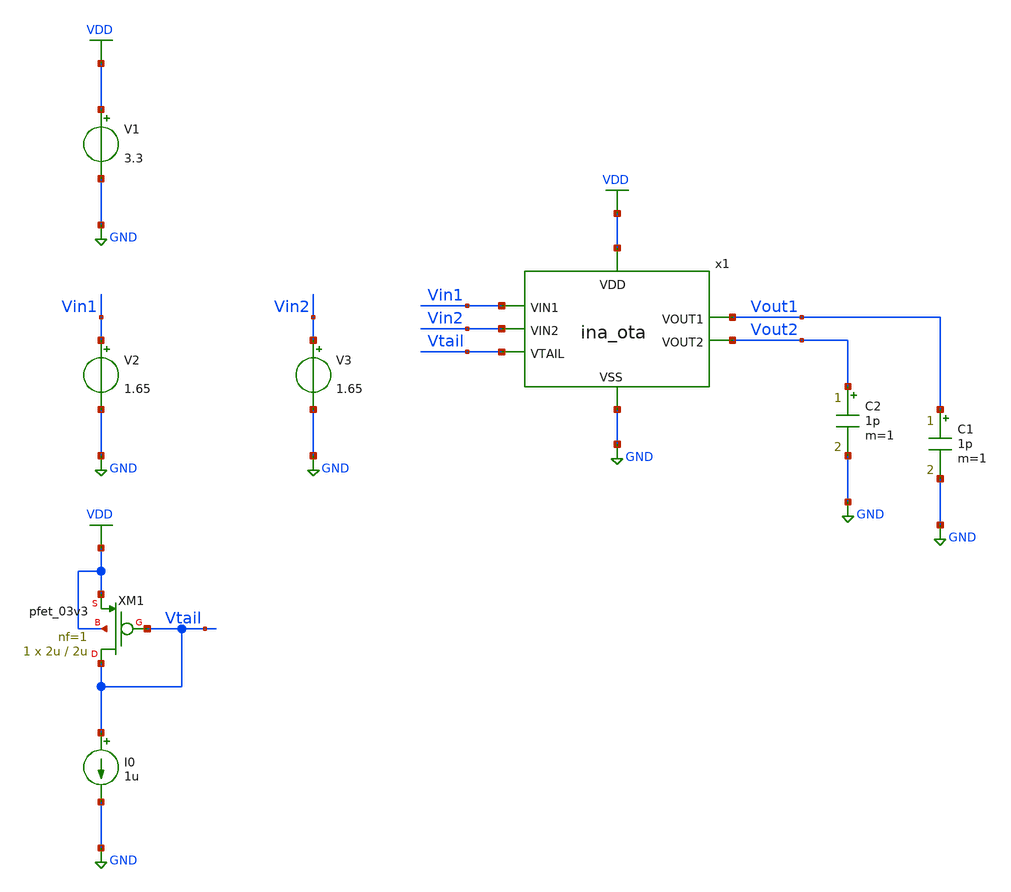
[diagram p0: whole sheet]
** sch_path: designs/libs/tb_ina/tb_ina_ota_tran/tb_ina_ota_tran.sch
**.subckt tb_ina_ota_tran
V1 VDD GND 3.3
V2 Vin1 GND 1.65
V3 Vin2 GND 1.65
C2 Vout2 GND 1p m=1
C1 Vout1 GND 1p m=1
XM1 Vtail Vtail VDD VDD pfet_03v3 L=2u W=2u nf=1 ad='int((nf+1)/2) * W/nf * 0.18u' as='int((nf+2)/2) * W/nf * 0.18u'
+ pd='2*int((nf+1)/2) * (W/nf + 0.18u)' ps='2*int((nf+2)/2) * (W/nf + 0.18u)' nrd='0.18u / W' nrs='0.18u / W'
+ sa=0 sb=0 sd=0 m=1
I0 Vtail GND 1u
x1 VDD Vtail Vin1 Vout2 Vout1 Vin2 GND ina_ota
**** begin user architecture code

.include $::180MCU_MODELS/design.ngspice
.lib $::180MCU_MODELS/sm141064.ngspice typical
.lib $::180MCU_MODELS/sm141064.ngspice cap_mim
.lib $::180MCU_MODELS/sm141064.ngspice moscap_typical
.lib $::180MCU_MODELS/sm141064.ngspice mimcap_typical
.lib $::180MCU_MODELS/sm141064.ngspice res_typical
* .lib $::180MCU_MODELS/sm141064.ngspice res_statistical
* ngspice commands




.control
save all

run
set color0 = white

*************************************
** ECG INPUT PARAMETERS
*************************************

let Vdd  = 3.3
let Vcm  = 1.65
let Vamp = 0.5m
let fecg = 100

*************************************
** BIAS PARAMETERS
*************************************

let Ibias = 2u

*************************************
** TRANSIENT PARAMETERS
*************************************

let tstop = 20m
let tstep = 1u

*************************************
** SOURCES
*************************************

alter @V1[DC] = $&Vdd
alter @V2[SIN] = [ $&Vcm $&Vamp $&fecg ]
alter @V3[SIN] = [ $&Vcm -$&Vamp $&fecg ]
alter @I0[DC] = $&Ibias

*************************************
** TRANSIENT SIMULATION
*************************************

tran $&tstep $&tstop

*************************************
** PLOTS
*************************************

setplot tran1
let vin_diff  = v(Vin1)-v(Vin2)
let vout_diff = v(Vout1)-v(Vout2)
let vin1 = v(Vin1)
let vin2 = v(Vin2)
let vout1 = v(Vout1)
let vout2 = v(Vout2)
plot vin_diff
plot vout_diff
plot vin1 vin2
plot vout1 vout2

*************************************
** SAVE
*************************************

write tb_ina_ota_tran.raw


.endc
* ngspice commands



**** end user architecture code
**.ends

* expanding   symbol:  libs/core_ina/ina_ota/ina_ota.sym # of pins=7
** sym_path: designs/libs/core_ina/ina_ota/ina_ota.sym
** sch_path: designs/libs/core_ina/ina_ota/ina_ota.sch
.subckt ina_ota VDD VTAIL VIN1 VOUT2 VOUT1 VIN2 VSS
*.ipin Vin1
*.ipin Vin2
*.ipin Vtail
*.ipin VSS
*.opin Vout1
*.ipin VDD
*.opin Vout2
XM2 net4 net4 VDD VDD pfet_03v3 L=6u W=0.65u nf=1 ad='int((nf+1)/2) * W/nf * 0.18u' as='int((nf+2)/2) * W/nf * 0.18u'
+ pd='2*int((nf+1)/2) * (W/nf + 0.18u)' ps='2*int((nf+2)/2) * (W/nf + 0.18u)' nrd='0.18u / W' nrs='0.18u / W'
+ sa=0 sb=0 sd=0 m=1
XM1 net3 Vtail VDD VDD pfet_03v3 L=2u W=8u nf=1 ad='int((nf+1)/2) * W/nf * 0.18u' as='int((nf+2)/2) * W/nf * 0.18u'
+ pd='2*int((nf+1)/2) * (W/nf + 0.18u)' ps='2*int((nf+2)/2) * (W/nf + 0.18u)' nrd='0.18u / W' nrs='0.18u / W'
+ sa=0 sb=0 sd=0 m=1
XM3 net5 net5 VDD VDD pfet_03v3 L=6u W=0.65u nf=1 ad='int((nf+1)/2) * W/nf * 0.18u' as='int((nf+2)/2) * W/nf * 0.18u'
+ pd='2*int((nf+1)/2) * (W/nf + 0.18u)' ps='2*int((nf+2)/2) * (W/nf + 0.18u)' nrd='0.18u / W' nrs='0.18u / W'
+ sa=0 sb=0 sd=0 m=1
XM4 net1 Vin1 net3 VDD pfet_03v3 L=0.28u W=15u nf=1 ad='int((nf+1)/2) * W/nf * 0.18u' as='int((nf+2)/2) * W/nf * 0.18u'
+ pd='2*int((nf+1)/2) * (W/nf + 0.18u)' ps='2*int((nf+2)/2) * (W/nf + 0.18u)' nrd='0.18u / W' nrs='0.18u / W'
+ sa=0 sb=0 sd=0 m=10
XM5 net2 Vin2 net3 VDD pfet_03v3 L=0.28u W=15u nf=1 ad='int((nf+1)/2) * W/nf * 0.18u' as='int((nf+2)/2) * W/nf * 0.18u'
+ pd='2*int((nf+1)/2) * (W/nf + 0.18u)' ps='2*int((nf+2)/2) * (W/nf + 0.18u)' nrd='0.18u / W' nrs='0.18u / W'
+ sa=0 sb=0 sd=0 m=10
XM6 net4 net1 VSS VSS nfet_03v3 L=6u W=1.8u nf=1 ad='int((nf+1)/2) * W/nf * 0.18u' as='int((nf+2)/2) * W/nf * 0.18u'
+ pd='2*int((nf+1)/2) * (W/nf + 0.18u)' ps='2*int((nf+2)/2) * (W/nf + 0.18u)' nrd='0.18u / W' nrs='0.18u / W'
+ sa=0 sb=0 sd=0 m=1
XM7 net5 net2 VSS VSS nfet_03v3 L=6u W=1.8u nf=1 ad='int((nf+1)/2) * W/nf * 0.18u' as='int((nf+2)/2) * W/nf * 0.18u'
+ pd='2*int((nf+1)/2) * (W/nf + 0.18u)' ps='2*int((nf+2)/2) * (W/nf + 0.18u)' nrd='0.18u / W' nrs='0.18u / W'
+ sa=0 sb=0 sd=0 m=1
XM8 net1 net1 VSS VSS nfet_03v3 L=6u W=1.8u nf=1 ad='int((nf+1)/2) * W/nf * 0.18u' as='int((nf+2)/2) * W/nf * 0.18u'
+ pd='2*int((nf+1)/2) * (W/nf + 0.18u)' ps='2*int((nf+2)/2) * (W/nf + 0.18u)' nrd='0.18u / W' nrs='0.18u / W'
+ sa=0 sb=0 sd=0 m=1
XM9 net2 net2 VSS VSS nfet_03v3 L=6u W=1.8u nf=1 ad='int((nf+1)/2) * W/nf * 0.18u' as='int((nf+2)/2) * W/nf * 0.18u'
+ pd='2*int((nf+1)/2) * (W/nf + 0.18u)' ps='2*int((nf+2)/2) * (W/nf + 0.18u)' nrd='0.18u / W' nrs='0.18u / W'
+ sa=0 sb=0 sd=0 m=1
XM10 Vout1 net4 VDD VDD pfet_03v3 L=6u W=0.65u nf=1 ad='int((nf+1)/2) * W/nf * 0.18u' as='int((nf+2)/2) * W/nf * 0.18u'
+ pd='2*int((nf+1)/2) * (W/nf + 0.18u)' ps='2*int((nf+2)/2) * (W/nf + 0.18u)' nrd='0.18u / W' nrs='0.18u / W'
+ sa=0 sb=0 sd=0 m=1
XM11 Vout1 net2 VSS VSS nfet_03v3 L=6u W=1.8u nf=1 ad='int((nf+1)/2) * W/nf * 0.18u' as='int((nf+2)/2) * W/nf * 0.18u'
+ pd='2*int((nf+1)/2) * (W/nf + 0.18u)' ps='2*int((nf+2)/2) * (W/nf + 0.18u)' nrd='0.18u / W' nrs='0.18u / W'
+ sa=0 sb=0 sd=0 m=1
XM12 Vout2 net1 VSS VSS nfet_03v3 L=6u W=1.8u nf=1 ad='int((nf+1)/2) * W/nf * 0.18u' as='int((nf+2)/2) * W/nf * 0.18u'
+ pd='2*int((nf+1)/2) * (W/nf + 0.18u)' ps='2*int((nf+2)/2) * (W/nf + 0.18u)' nrd='0.18u / W' nrs='0.18u / W'
+ sa=0 sb=0 sd=0 m=1
XM13 Vout2 net5 VDD VDD pfet_03v3 L=6u W=0.65u nf=1 ad='int((nf+1)/2) * W/nf * 0.18u' as='int((nf+2)/2) * W/nf * 0.18u'
+ pd='2*int((nf+1)/2) * (W/nf + 0.18u)' ps='2*int((nf+2)/2) * (W/nf + 0.18u)' nrd='0.18u / W' nrs='0.18u / W'
+ sa=0 sb=0 sd=0 m=1
.ends

.GLOBAL GND
.GLOBAL VDD
.end
